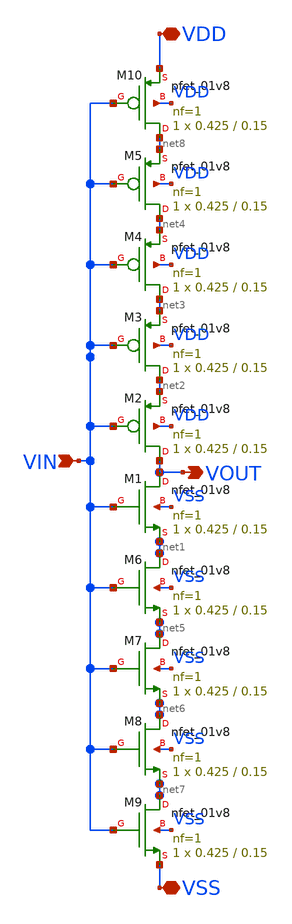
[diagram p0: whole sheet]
** sch_path: xschem/DC_DC_Converter_xschem/OTHERS/DC_DC_Converter_3/Inverter_64X/Inverter_64.sch
**.subckt Inverter_64 VIN VDD VSS VOUT
*.ipin VIN
*.iopin VDD
*.iopin VSS
*.opin VOUT
XM1 VOUT VIN net1 VSS sky130_fd_pr__nfet_01v8 L=0.15 W=0.425 nf=1 ad='int((nf+1)/2) * W/nf * 0.29' as='int((nf+2)/2) * W/nf * 0.29'
+ pd='2*int((nf+1)/2) * (W/nf + 0.29)' ps='2*int((nf+2)/2) * (W/nf + 0.29)' nrd='0.29 / W' nrs='0.29 / W'
+ sa=0 sb=0 sd=0 mult=1 m=1
XM2 VOUT VIN net2 VDD sky130_fd_pr__pfet_01v8 L=0.15 W=0.425 nf=1 ad='int((nf+1)/2) * W/nf * 0.29' as='int((nf+2)/2) * W/nf * 0.29'
+ pd='2*int((nf+1)/2) * (W/nf + 0.29)' ps='2*int((nf+2)/2) * (W/nf + 0.29)' nrd='0.29 / W' nrs='0.29 / W'
+ sa=0 sb=0 sd=0 mult=1 m=1
XM3 net2 VIN net3 VDD sky130_fd_pr__pfet_01v8 L=0.15 W=0.425 nf=1 ad='int((nf+1)/2) * W/nf * 0.29' as='int((nf+2)/2) * W/nf * 0.29'
+ pd='2*int((nf+1)/2) * (W/nf + 0.29)' ps='2*int((nf+2)/2) * (W/nf + 0.29)' nrd='0.29 / W' nrs='0.29 / W'
+ sa=0 sb=0 sd=0 mult=1 m=1
XM4 net3 VIN net4 VDD sky130_fd_pr__pfet_01v8 L=0.15 W=0.425 nf=1 ad='int((nf+1)/2) * W/nf * 0.29' as='int((nf+2)/2) * W/nf * 0.29'
+ pd='2*int((nf+1)/2) * (W/nf + 0.29)' ps='2*int((nf+2)/2) * (W/nf + 0.29)' nrd='0.29 / W' nrs='0.29 / W'
+ sa=0 sb=0 sd=0 mult=1 m=1
XM5 net4 VIN net8 VDD sky130_fd_pr__pfet_01v8 L=0.15 W=0.425 nf=1 ad='int((nf+1)/2) * W/nf * 0.29' as='int((nf+2)/2) * W/nf * 0.29'
+ pd='2*int((nf+1)/2) * (W/nf + 0.29)' ps='2*int((nf+2)/2) * (W/nf + 0.29)' nrd='0.29 / W' nrs='0.29 / W'
+ sa=0 sb=0 sd=0 mult=1 m=1
XM6 net1 VIN net5 VSS sky130_fd_pr__nfet_01v8 L=0.15 W=0.425 nf=1 ad='int((nf+1)/2) * W/nf * 0.29' as='int((nf+2)/2) * W/nf * 0.29'
+ pd='2*int((nf+1)/2) * (W/nf + 0.29)' ps='2*int((nf+2)/2) * (W/nf + 0.29)' nrd='0.29 / W' nrs='0.29 / W'
+ sa=0 sb=0 sd=0 mult=1 m=1
XM7 net5 VIN net6 VSS sky130_fd_pr__nfet_01v8 L=0.15 W=0.425 nf=1 ad='int((nf+1)/2) * W/nf * 0.29' as='int((nf+2)/2) * W/nf * 0.29'
+ pd='2*int((nf+1)/2) * (W/nf + 0.29)' ps='2*int((nf+2)/2) * (W/nf + 0.29)' nrd='0.29 / W' nrs='0.29 / W'
+ sa=0 sb=0 sd=0 mult=1 m=1
XM8 net6 VIN net7 VSS sky130_fd_pr__nfet_01v8 L=0.15 W=0.425 nf=1 ad='int((nf+1)/2) * W/nf * 0.29' as='int((nf+2)/2) * W/nf * 0.29'
+ pd='2*int((nf+1)/2) * (W/nf + 0.29)' ps='2*int((nf+2)/2) * (W/nf + 0.29)' nrd='0.29 / W' nrs='0.29 / W'
+ sa=0 sb=0 sd=0 mult=1 m=1
XM9 net7 VIN VSS VSS sky130_fd_pr__nfet_01v8 L=0.15 W=0.425 nf=1 ad='int((nf+1)/2) * W/nf * 0.29' as='int((nf+2)/2) * W/nf * 0.29'
+ pd='2*int((nf+1)/2) * (W/nf + 0.29)' ps='2*int((nf+2)/2) * (W/nf + 0.29)' nrd='0.29 / W' nrs='0.29 / W'
+ sa=0 sb=0 sd=0 mult=1 m=1
XM10 net8 VIN VDD VDD sky130_fd_pr__pfet_01v8 L=0.15 W=0.425 nf=1 ad='int((nf+1)/2) * W/nf * 0.29' as='int((nf+2)/2) * W/nf * 0.29'
+ pd='2*int((nf+1)/2) * (W/nf + 0.29)' ps='2*int((nf+2)/2) * (W/nf + 0.29)' nrd='0.29 / W' nrs='0.29 / W'
+ sa=0 sb=0 sd=0 mult=1 m=1
**** begin user architecture code

** opencircuitdesign pdks install
.lib $::SKYWATER_MODELS/sky130.lib.spice tt


**** end user architecture code
**.ends
.end
